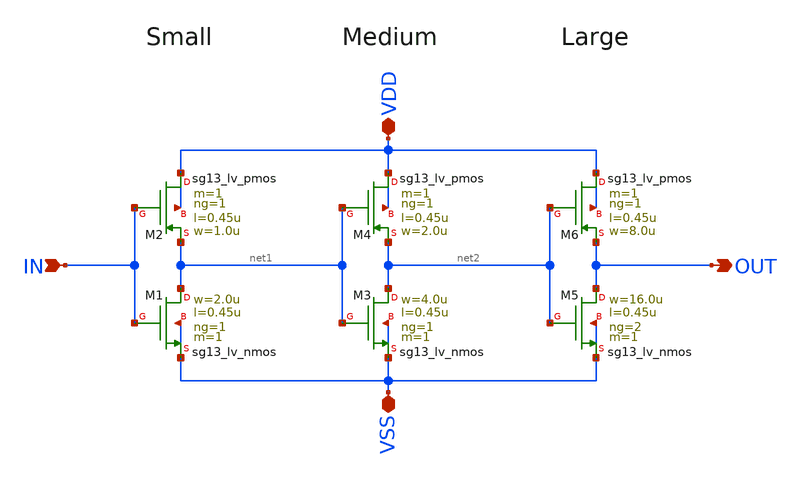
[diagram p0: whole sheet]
** sch_path: analog/output_buffer_chain/output_buffer_chain.sch
**.subckt output_buffer_chain IN OUT VDD VSS
*.ipin IN
*.opin OUT
*.iopin VDD
*.iopin VSS
XM1 net1 IN VSS VSS sg13_lv_nmos w=2.0u l=0.45u ng=1 m=1 mm_ok=1
XM2 VDD IN net1 VDD sg13_lv_pmos w=1.0u l=0.45u ng=1 m=1 mm_ok=1
XM3 net2 net1 VSS VSS sg13_lv_nmos w=4.0u l=0.45u ng=1 m=1 mm_ok=1
XM4 VDD net1 net2 VDD sg13_lv_pmos w=2.0u l=0.45u ng=1 m=1 mm_ok=1
XM5 OUT net2 VSS VSS sg13_lv_nmos w=16.0u l=0.45u ng=2 m=1 mm_ok=1
XM6 VDD net2 OUT VDD sg13_lv_pmos w=8.0u l=0.45u ng=1 m=1 mm_ok=1
**.ends
.end
